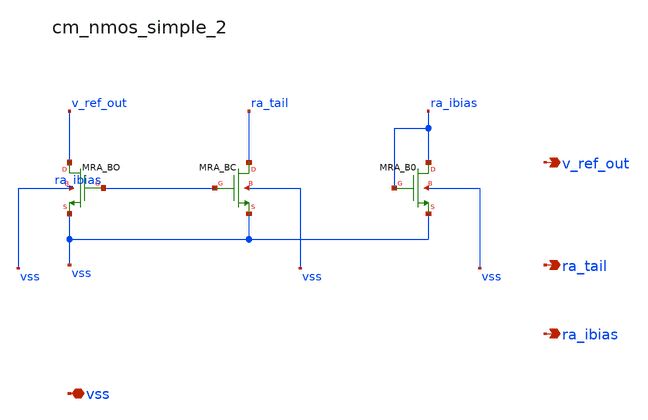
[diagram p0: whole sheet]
** sch_path: analog-db/raw/ldo_005_buffered_ref/hier/blocks/cm_nmos_simple_2.sch
**.subckt cm_nmos_simple_2 vss v_ref_out ra_tail ra_ibias
*.iopin vss
*.opin v_ref_out
*.opin ra_tail
*.opin ra_ibias
XMRA_B0 ra_ibias ra_ibias vss vss sg13_hv_nmos w=x_dut_xmra_b0_w l=x_dut_xmra_b0_l ng=1 m=1
XMRA_BC ra_tail ra_ibias vss vss sg13_hv_nmos w=x_dut_xmra_bc_w l=x_dut_xmra_bc_l ng=1 m=1
XMRA_BO v_ref_out ra_ibias vss vss sg13_hv_nmos w=x_dut_xmra_bo_w l=x_dut_xmra_bo_l ng=1 m=1
**.ends
.end
